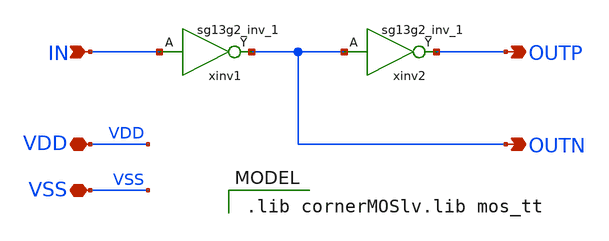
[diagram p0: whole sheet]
** sch_path: xschem/inverterpair.sch
**.subckt inverterpair VSS IN OUTN OUTP VDD
*.iopin VSS
*.ipin IN
*.opin OUTN
*.opin OUTP
*.iopin VDD
xinv2 OUTP OUTN VDD VSS sg13g2_inv_1
xinv1 OUTN IN VDD VSS sg13g2_inv_1
**** begin user architecture code
 .lib cornerMOSlv.lib mos_tt

**** end user architecture code
**.ends

* expanding   symbol:  sg13g2_stdcells/sg13g2_inv_1.sym # of pins=2
** sym_path: sg13g2_stdcells/sg13g2_inv_1.sym
** sch_path: sg13g2_stdcells/sg13g2_inv_1.sch
.subckt sg13g2_inv_1 Y A VDD VSS
*.opin Y
*.ipin A
*.iopin VDD
*.iopin VSS
XM1 Y A VSS VSS sg13_lv_nmos w=740.00n l=130.00n ng=1 m=1 mm_ok=1
XM2 Y A VDD VDD sg13_lv_pmos w=1.12u l=130.00n ng=1 m=1 mm_ok=1
.ends

.end
